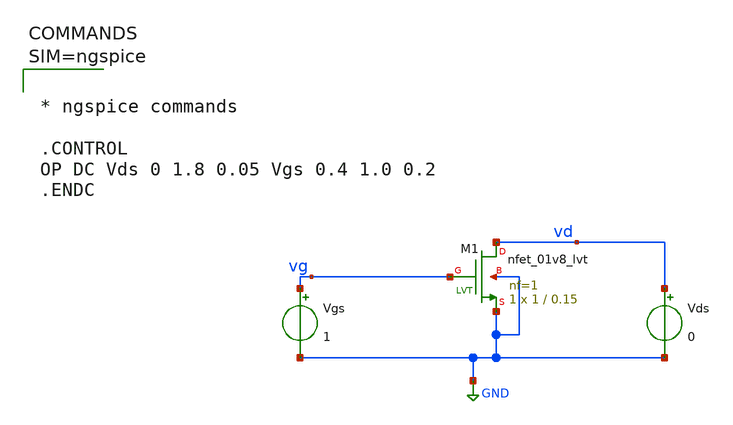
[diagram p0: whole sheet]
** sch_path: work/xschem/untitled-2.sch
**.subckt untitled-2
XM1 vd vg GND GND sky130_fd_pr__nfet_01v8_lvt L=0.15 W=1 nf=1 ad='int((1 + 1)/2) * 1 / 1 * 0.29' as='int((1 + 2)/2) * 1 / 1 * 0.29'
+ pd='2*int((1 + 1)/2) * (1 / 1 + 0.29)' ps='2*int((1 + 2)/2) * (1 / 1 + 0.29)' nrd='0.29 / 1 ' nrs='0.29 / 1 '
+ sa=0 sb=0 sd=0 mult=1 m=1
Vgs vg GND 1
Vds vd GND 0
**** begin user architecture code



* ngspice commands

.CONTROL
OP DC Vds 0 1.8 0.05 Vgs 0.4 1.0 0.2
.ENDC




** opencircuitdesign pdks install
.lib $::SKYWATER_MODELS/sky130.lib.spice tt

**** end user architecture code
**.ends
.GLOBAL GND
.end
